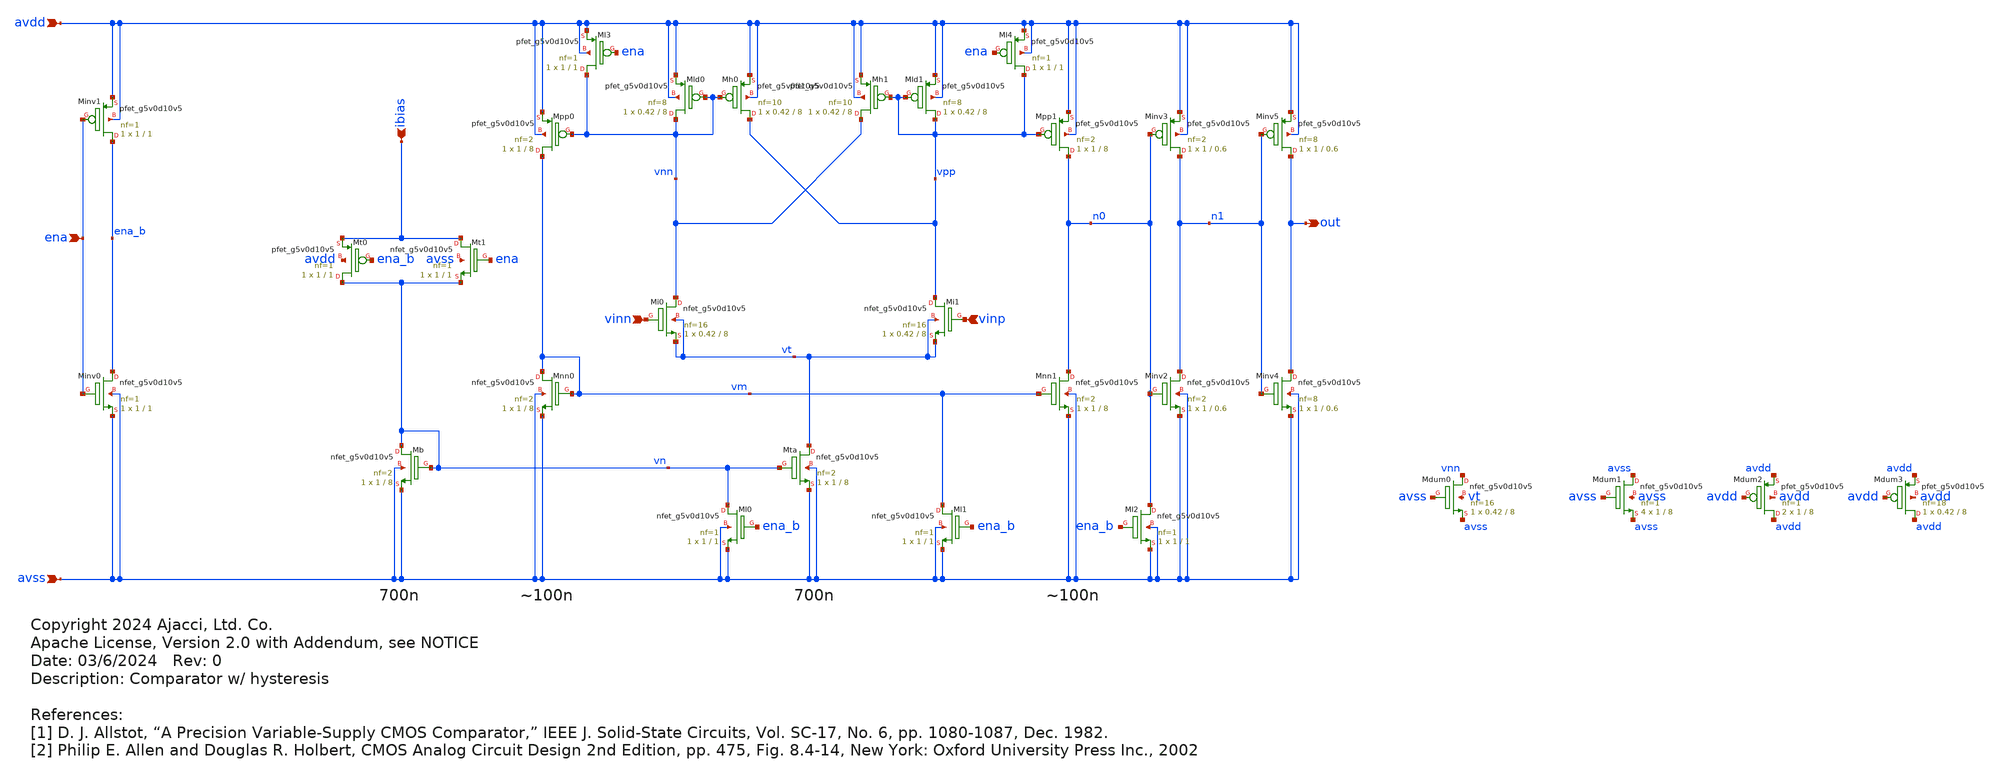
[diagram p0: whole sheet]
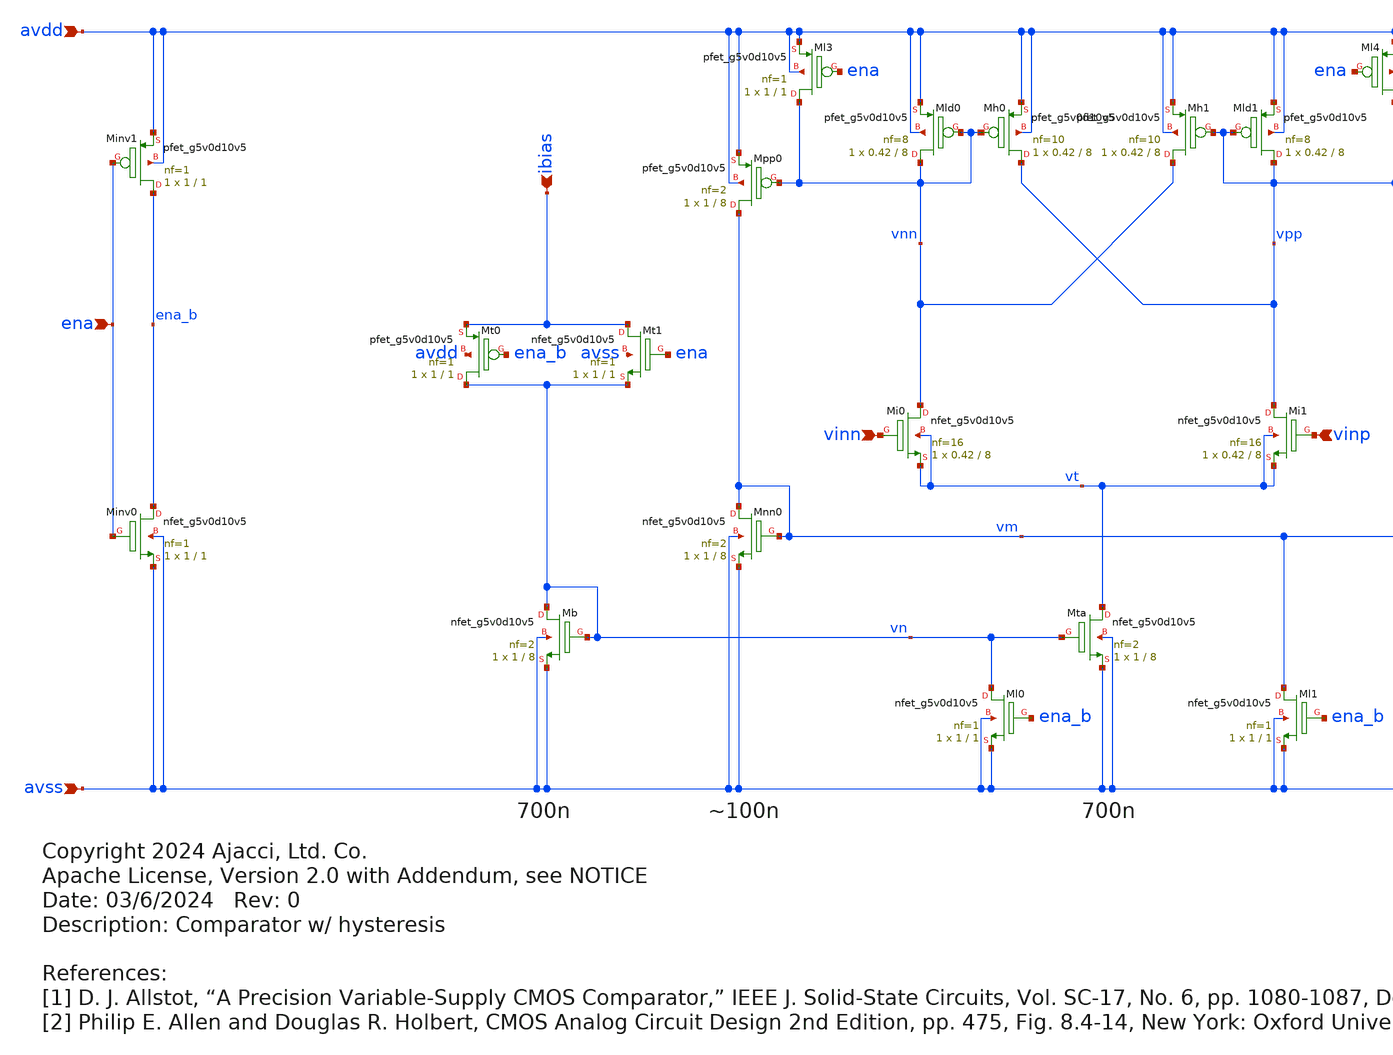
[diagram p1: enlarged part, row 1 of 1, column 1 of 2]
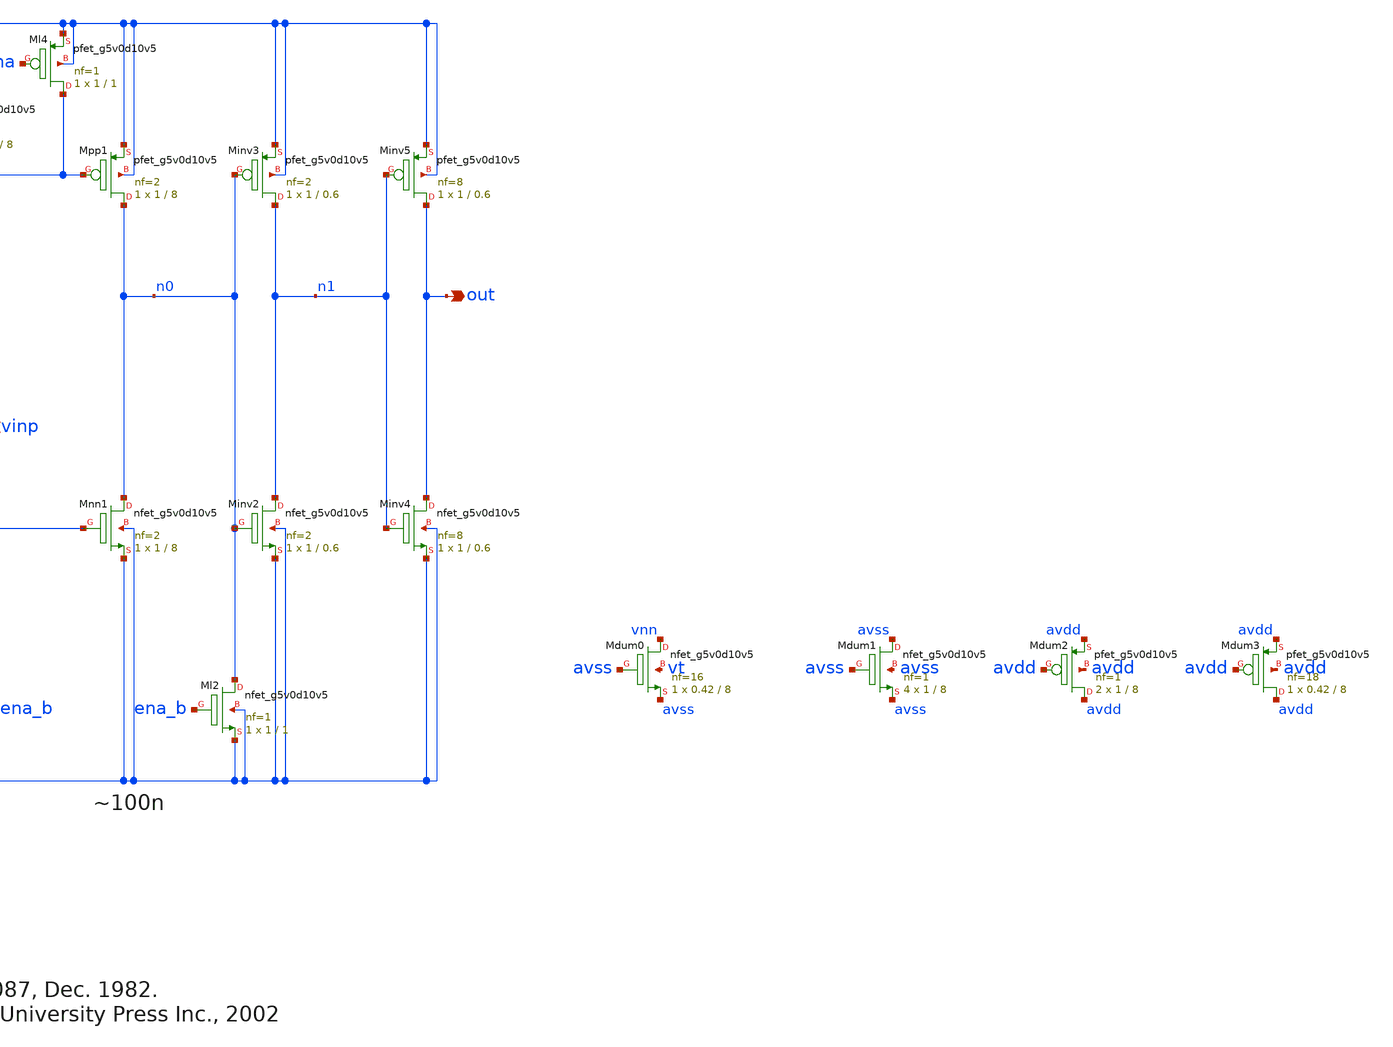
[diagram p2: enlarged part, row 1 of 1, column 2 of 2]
** sch_path: xschem/comparator.sch
* Copyright 2024 Ajacci, Ltd. Co.
* Apache License, Version 2.0 with Addendum, see NOTICE
**.subckt comparator ena avdd avss ibias vinn vinp out
*.ipin ena
*.ipin avdd
*.ipin avss
*.ipin ibias
*.ipin vinn
*.ipin vinp
*.opin out
XMb vn vn avss avss sky130_fd_pr__nfet_g5v0d10v5 L=8 W=1 nf=2 ad='int((nf+1)/2) * W/nf * 0.29' as='int((nf+2)/2) * W/nf * 0.29'
+ pd='2*int((nf+1)/2) * (W/nf + 0.29)' ps='2*int((nf+2)/2) * (W/nf + 0.29)' nrd='0.29 / W' nrs='0.29 / W'
+ sa=0 sb=0 sd=0 mult=1 m=1
XMta vt vn avss avss sky130_fd_pr__nfet_g5v0d10v5 L=8 W=1 nf=2 ad='int((nf+1)/2) * W/nf * 0.29' as='int((nf+2)/2) * W/nf * 0.29'
+ pd='2*int((nf+1)/2) * (W/nf + 0.29)' ps='2*int((nf+2)/2) * (W/nf + 0.29)' nrd='0.29 / W' nrs='0.29 / W'
+ sa=0 sb=0 sd=0 mult=1 m=1
XMl0 vn ena_b avss avss sky130_fd_pr__nfet_g5v0d10v5 L=1 W=1 nf=1 ad='int((nf+1)/2) * W/nf * 0.29' as='int((nf+2)/2) * W/nf * 0.29'
+ pd='2*int((nf+1)/2) * (W/nf + 0.29)' ps='2*int((nf+2)/2) * (W/nf + 0.29)' nrd='0.29 / W' nrs='0.29 / W'
+ sa=0 sb=0 sd=0 mult=1 m=1
XMinv0 ena_b ena avss avss sky130_fd_pr__nfet_g5v0d10v5 L=1 W=1 nf=1 ad='int((nf+1)/2) * W/nf * 0.29'
+ as='int((nf+2)/2) * W/nf * 0.29' pd='2*int((nf+1)/2) * (W/nf + 0.29)' ps='2*int((nf+2)/2) * (W/nf + 0.29)'
+ nrd='0.29 / W' nrs='0.29 / W' sa=0 sb=0 sd=0 mult=1 m=1
XMinv1 ena_b ena avdd avdd sky130_fd_pr__pfet_g5v0d10v5 L=1 W=1 nf=1 ad='int((nf+1)/2) * W/nf * 0.29'
+ as='int((nf+2)/2) * W/nf * 0.29' pd='2*int((nf+1)/2) * (W/nf + 0.29)' ps='2*int((nf+2)/2) * (W/nf + 0.29)'
+ nrd='0.29 / W' nrs='0.29 / W' sa=0 sb=0 sd=0 mult=1 m=1
XMi0 vnn vinn vt vt sky130_fd_pr__nfet_g5v0d10v5 L=8 W=0.42 nf=16 ad='int((nf+1)/2) * W/nf * 0.29' as='int((nf+2)/2) * W/nf * 0.29'
+ pd='2*int((nf+1)/2) * (W/nf + 0.29)' ps='2*int((nf+2)/2) * (W/nf + 0.29)' nrd='0.29 / W' nrs='0.29 / W'
+ sa=0 sb=0 sd=0 mult=1 m=1
XMi1 vpp vinp vt vt sky130_fd_pr__nfet_g5v0d10v5 L=8 W=0.42 nf=16 ad='int((nf+1)/2) * W/nf * 0.29' as='int((nf+2)/2) * W/nf * 0.29'
+ pd='2*int((nf+1)/2) * (W/nf + 0.29)' ps='2*int((nf+2)/2) * (W/nf + 0.29)' nrd='0.29 / W' nrs='0.29 / W'
+ sa=0 sb=0 sd=0 mult=1 m=1
XMld1 vpp vpp avdd avdd sky130_fd_pr__pfet_g5v0d10v5 L=8 W=0.42 nf=8 ad='int((nf+1)/2) * W/nf * 0.29'
+ as='int((nf+2)/2) * W/nf * 0.29' pd='2*int((nf+1)/2) * (W/nf + 0.29)' ps='2*int((nf+2)/2) * (W/nf + 0.29)'
+ nrd='0.29 / W' nrs='0.29 / W' sa=0 sb=0 sd=0 mult=1 m=1
XMh1 vnn vpp avdd avdd sky130_fd_pr__pfet_g5v0d10v5 L=8 W=0.42 nf=10 ad='int((nf+1)/2) * W/nf * 0.29'
+ as='int((nf+2)/2) * W/nf * 0.29' pd='2*int((nf+1)/2) * (W/nf + 0.29)' ps='2*int((nf+2)/2) * (W/nf + 0.29)'
+ nrd='0.29 / W' nrs='0.29 / W' sa=0 sb=0 sd=0 mult=1 m=1
XMh0 vpp vnn avdd avdd sky130_fd_pr__pfet_g5v0d10v5 L=8 W=0.42 nf=10 ad='int((nf+1)/2) * W/nf * 0.29'
+ as='int((nf+2)/2) * W/nf * 0.29' pd='2*int((nf+1)/2) * (W/nf + 0.29)' ps='2*int((nf+2)/2) * (W/nf + 0.29)'
+ nrd='0.29 / W' nrs='0.29 / W' sa=0 sb=0 sd=0 mult=1 m=1
XMld0 vnn vnn avdd avdd sky130_fd_pr__pfet_g5v0d10v5 L=8 W=0.42 nf=8 ad='int((nf+1)/2) * W/nf * 0.29'
+ as='int((nf+2)/2) * W/nf * 0.29' pd='2*int((nf+1)/2) * (W/nf + 0.29)' ps='2*int((nf+2)/2) * (W/nf + 0.29)'
+ nrd='0.29 / W' nrs='0.29 / W' sa=0 sb=0 sd=0 mult=1 m=1
XMpp1 n0 vpp avdd avdd sky130_fd_pr__pfet_g5v0d10v5 L=8 W=1 nf=2 ad='int((nf+1)/2) * W/nf * 0.29' as='int((nf+2)/2) * W/nf * 0.29'
+ pd='2*int((nf+1)/2) * (W/nf + 0.29)' ps='2*int((nf+2)/2) * (W/nf + 0.29)' nrd='0.29 / W' nrs='0.29 / W'
+ sa=0 sb=0 sd=0 mult=1 m=1
XMnn1 n0 vm avss avss sky130_fd_pr__nfet_g5v0d10v5 L=8 W=1 nf=2 ad='int((nf+1)/2) * W/nf * 0.29' as='int((nf+2)/2) * W/nf * 0.29'
+ pd='2*int((nf+1)/2) * (W/nf + 0.29)' ps='2*int((nf+2)/2) * (W/nf + 0.29)' nrd='0.29 / W' nrs='0.29 / W'
+ sa=0 sb=0 sd=0 mult=1 m=1
XMpp0 vm vnn avdd avdd sky130_fd_pr__pfet_g5v0d10v5 L=8 W=1 nf=2 ad='int((nf+1)/2) * W/nf * 0.29' as='int((nf+2)/2) * W/nf * 0.29'
+ pd='2*int((nf+1)/2) * (W/nf + 0.29)' ps='2*int((nf+2)/2) * (W/nf + 0.29)' nrd='0.29 / W' nrs='0.29 / W'
+ sa=0 sb=0 sd=0 mult=1 m=1
XMnn0 vm vm avss avss sky130_fd_pr__nfet_g5v0d10v5 L=8 W=1 nf=2 ad='int((nf+1)/2) * W/nf * 0.29' as='int((nf+2)/2) * W/nf * 0.29'
+ pd='2*int((nf+1)/2) * (W/nf + 0.29)' ps='2*int((nf+2)/2) * (W/nf + 0.29)' nrd='0.29 / W' nrs='0.29 / W'
+ sa=0 sb=0 sd=0 mult=1 m=1
XMinv3 n1 n0 avdd avdd sky130_fd_pr__pfet_g5v0d10v5 L=0.6 W=1 nf=2 ad='int((nf+1)/2) * W/nf * 0.29' as='int((nf+2)/2) * W/nf * 0.29'
+ pd='2*int((nf+1)/2) * (W/nf + 0.29)' ps='2*int((nf+2)/2) * (W/nf + 0.29)' nrd='0.29 / W' nrs='0.29 / W'
+ sa=0 sb=0 sd=0 mult=1 m=1
XMinv2 n1 n0 avss avss sky130_fd_pr__nfet_g5v0d10v5 L=0.6 W=1 nf=2 ad='int((nf+1)/2) * W/nf * 0.29' as='int((nf+2)/2) * W/nf * 0.29'
+ pd='2*int((nf+1)/2) * (W/nf + 0.29)' ps='2*int((nf+2)/2) * (W/nf + 0.29)' nrd='0.29 / W' nrs='0.29 / W'
+ sa=0 sb=0 sd=0 mult=1 m=1
XMinv5 out n1 avdd avdd sky130_fd_pr__pfet_g5v0d10v5 L=0.6 W=1 nf=8 ad='int((nf+1)/2) * W/nf * 0.29'
+ as='int((nf+2)/2) * W/nf * 0.29' pd='2*int((nf+1)/2) * (W/nf + 0.29)' ps='2*int((nf+2)/2) * (W/nf + 0.29)'
+ nrd='0.29 / W' nrs='0.29 / W' sa=0 sb=0 sd=0 mult=1 m=1
XMinv4 out n1 avss avss sky130_fd_pr__nfet_g5v0d10v5 L=0.6 W=1 nf=8 ad='int((nf+1)/2) * W/nf * 0.29'
+ as='int((nf+2)/2) * W/nf * 0.29' pd='2*int((nf+1)/2) * (W/nf + 0.29)' ps='2*int((nf+2)/2) * (W/nf + 0.29)'
+ nrd='0.29 / W' nrs='0.29 / W' sa=0 sb=0 sd=0 mult=1 m=1
XMl1 vm ena_b avss avss sky130_fd_pr__nfet_g5v0d10v5 L=1 W=1 nf=1 ad='int((nf+1)/2) * W/nf * 0.29' as='int((nf+2)/2) * W/nf * 0.29'
+ pd='2*int((nf+1)/2) * (W/nf + 0.29)' ps='2*int((nf+2)/2) * (W/nf + 0.29)' nrd='0.29 / W' nrs='0.29 / W'
+ sa=0 sb=0 sd=0 mult=1 m=1
XMl3 vnn ena avdd avdd sky130_fd_pr__pfet_g5v0d10v5 L=1 W=1 nf=1 ad='int((nf+1)/2) * W/nf * 0.29' as='int((nf+2)/2) * W/nf * 0.29'
+ pd='2*int((nf+1)/2) * (W/nf + 0.29)' ps='2*int((nf+2)/2) * (W/nf + 0.29)' nrd='0.29 / W' nrs='0.29 / W'
+ sa=0 sb=0 sd=0 mult=1 m=1
XMl4 vpp ena avdd avdd sky130_fd_pr__pfet_g5v0d10v5 L=1 W=1 nf=1 ad='int((nf+1)/2) * W/nf * 0.29' as='int((nf+2)/2) * W/nf * 0.29'
+ pd='2*int((nf+1)/2) * (W/nf + 0.29)' ps='2*int((nf+2)/2) * (W/nf + 0.29)' nrd='0.29 / W' nrs='0.29 / W'
+ sa=0 sb=0 sd=0 mult=1 m=1
XMt1 ibias ena vn avss sky130_fd_pr__nfet_g5v0d10v5 L=1 W=1 nf=1 ad='int((nf+1)/2) * W/nf * 0.29' as='int((nf+2)/2) * W/nf * 0.29'
+ pd='2*int((nf+1)/2) * (W/nf + 0.29)' ps='2*int((nf+2)/2) * (W/nf + 0.29)' nrd='0.29 / W' nrs='0.29 / W'
+ sa=0 sb=0 sd=0 mult=1 m=1
XMt0 vn ena_b ibias avdd sky130_fd_pr__pfet_g5v0d10v5 L=1 W=1 nf=1 ad='int((nf+1)/2) * W/nf * 0.29' as='int((nf+2)/2) * W/nf * 0.29'
+ pd='2*int((nf+1)/2) * (W/nf + 0.29)' ps='2*int((nf+2)/2) * (W/nf + 0.29)' nrd='0.29 / W' nrs='0.29 / W'
+ sa=0 sb=0 sd=0 mult=1 m=1
XMl2 n0 ena_b avss avss sky130_fd_pr__nfet_g5v0d10v5 L=1 W=1 nf=1 ad='int((nf+1)/2) * W/nf * 0.29' as='int((nf+2)/2) * W/nf * 0.29'
+ pd='2*int((nf+1)/2) * (W/nf + 0.29)' ps='2*int((nf+2)/2) * (W/nf + 0.29)' nrd='0.29 / W' nrs='0.29 / W'
+ sa=0 sb=0 sd=0 mult=1 m=1
XMdum0 vnn avss avss vt sky130_fd_pr__nfet_g5v0d10v5 L=8 W=0.42 nf=16 ad='int((nf+1)/2) * W/nf * 0.29'
+ as='int((nf+2)/2) * W/nf * 0.29' pd='2*int((nf+1)/2) * (W/nf + 0.29)' ps='2*int((nf+2)/2) * (W/nf + 0.29)'
+ nrd='0.29 / W' nrs='0.29 / W' sa=0 sb=0 sd=0 mult=1 m=1
XMdum1 avss avss avss avss sky130_fd_pr__nfet_g5v0d10v5 L=8 W=1 nf=1 ad='int((nf+1)/2) * W/nf * 0.29'
+ as='int((nf+2)/2) * W/nf * 0.29' pd='2*int((nf+1)/2) * (W/nf + 0.29)' ps='2*int((nf+2)/2) * (W/nf + 0.29)'
+ nrd='0.29 / W' nrs='0.29 / W' sa=0 sb=0 sd=0 mult=4 m=4
XMdum2 avdd avdd avdd avdd sky130_fd_pr__pfet_g5v0d10v5 L=8 W=1 nf=1 ad='int((nf+1)/2) * W/nf * 0.29'
+ as='int((nf+2)/2) * W/nf * 0.29' pd='2*int((nf+1)/2) * (W/nf + 0.29)' ps='2*int((nf+2)/2) * (W/nf + 0.29)'
+ nrd='0.29 / W' nrs='0.29 / W' sa=0 sb=0 sd=0 mult=2 m=2
XMdum3 avdd avdd avdd avdd sky130_fd_pr__pfet_g5v0d10v5 L=8 W=0.42 nf=18 ad='int((nf+1)/2) * W/nf * 0.29'
+ as='int((nf+2)/2) * W/nf * 0.29' pd='2*int((nf+1)/2) * (W/nf + 0.29)' ps='2*int((nf+2)/2) * (W/nf + 0.29)'
+ nrd='0.29 / W' nrs='0.29 / W' sa=0 sb=0 sd=0 mult=1 m=1
**.ends
.end
